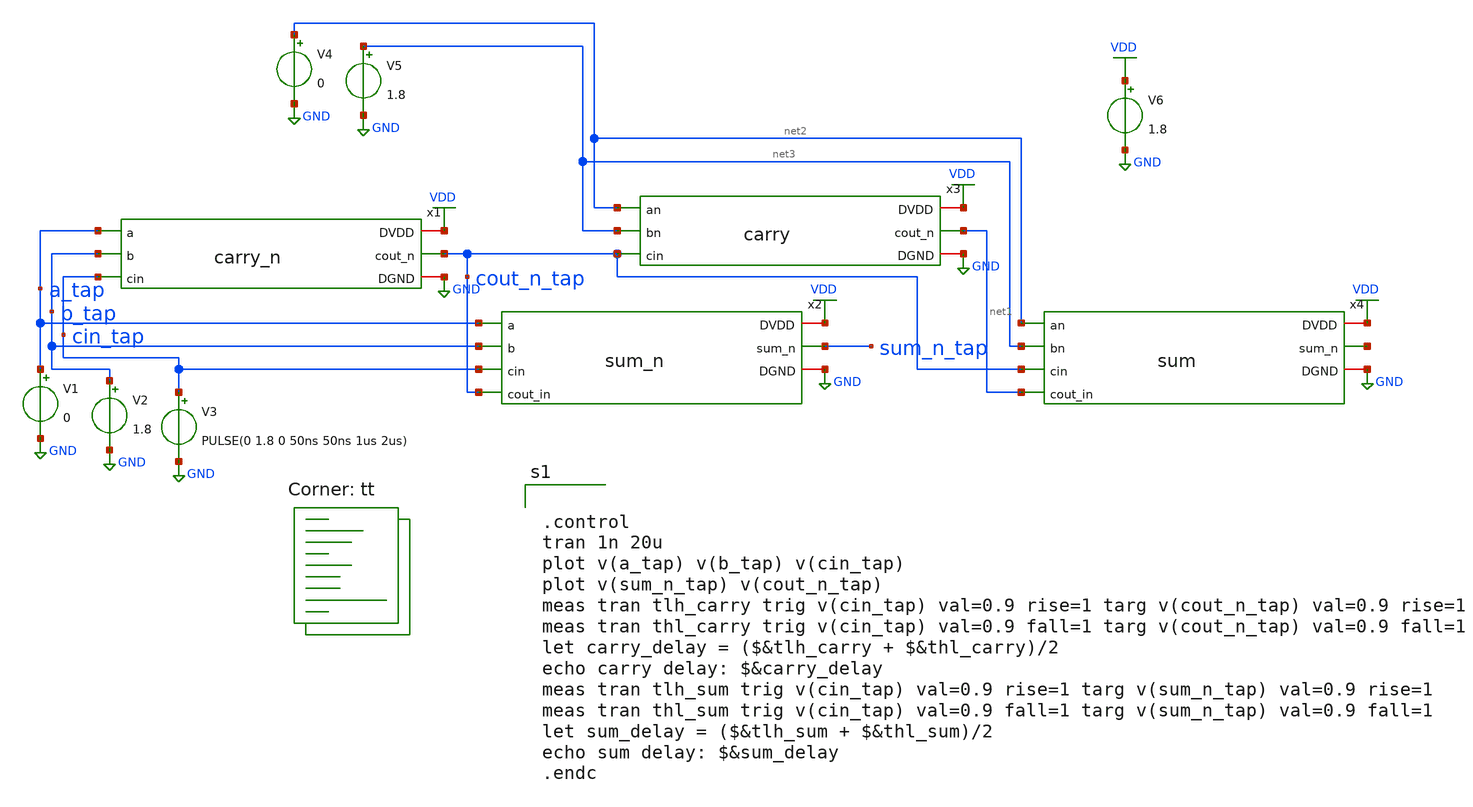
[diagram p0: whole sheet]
** sch_path: tut6/again_lf/sim/adder.sch
**.subckt adder
x1 VDD a_tap b_tap cout_n_tap cin_tap GND carry_n
x2 VDD a_tap b_tap sum_n_tap cin_tap cout_n_tap GND sum_n
x3 VDD net2 net3 net1 cout_n_tap GND carry
x4 VDD net2 net4 net3 cout_n_tap net1 GND sum
V1 a_tap GND 0
V2 b_tap GND 1.8
V3 cin_tap GND PULSE(0 1.8 0 50ns 50ns 1us 2us)
V4 net2 GND 0
V5 net3 GND 1.8
V6 VDD GND 1.8
**** begin user architecture code


.control
tran 1n 20u
plot v(a_tap) v(b_tap) v(cin_tap)
plot v(sum_n_tap) v(cout_n_tap)
meas tran tlh_carry trig v(cin_tap) val=0.9 rise=1 targ v(cout_n_tap) val=0.9 rise=1
meas tran thl_carry trig v(cin_tap) val=0.9 fall=1 targ v(cout_n_tap) val=0.9 fall=1
let carry_delay = ($&tlh_carry + $&thl_carry)/2
echo carry delay: $&carry_delay
meas tran tlh_sum trig v(cin_tap) val=0.9 rise=1 targ v(sum_n_tap) val=0.9 rise=1
meas tran thl_sum trig v(cin_tap) val=0.9 fall=1 targ v(sum_n_tap) val=0.9 fall=1
let sum_delay = ($&tlh_sum + $&thl_sum)/2
echo sum delay: $&sum_delay
.endc

.lib $::SKYWATER_MODELS/sky130.lib.spice tt
**** end user architecture code
**.ends
.GLOBAL VDD
.GLOBAL GND
.end
